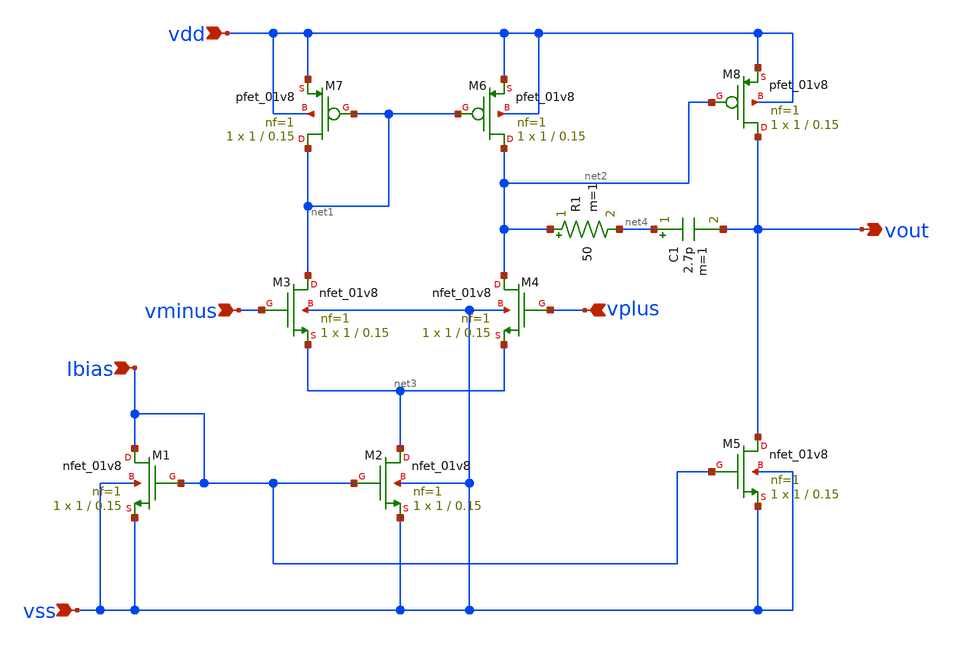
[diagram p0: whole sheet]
** sch_path: Primitives/Operational Amplifier/Xschem Files/sky130_opamp.sch
**.subckt sky130_opamp Ibias vminus vplus vss vdd vout
*.ipin Ibias
*.ipin vminus
*.ipin vplus
*.ipin vss
*.ipin vdd
*.opin vout
XM1 Ibias Ibias vss vss sky130_fd_pr__nfet_01v8 L=0.15 W=1 nf=1 ad='int((1 + 1)/2) * 1 / 1 * 0.29' as='int((1 + 2)/2) * 1 / 1 * 0.29'
+ pd='2*int((1 + 1)/2) * (1 / 1 + 0.29)' ps='2*int((1 + 2)/2) * (1 / 1 + 0.29)' nrd='0.29 / 1 ' nrs='0.29 / 1 '
+ sa=0 sb=0 sd=0 mult=1 m=1
XM2 net3 Ibias vss vss sky130_fd_pr__nfet_01v8 L=0.15 W=1 nf=1 ad='int((1 + 1)/2) * 1 / 1 * 0.29' as='int((1 + 2)/2) * 1 / 1 * 0.29'
+ pd='2*int((1 + 1)/2) * (1 / 1 + 0.29)' ps='2*int((1 + 2)/2) * (1 / 1 + 0.29)' nrd='0.29 / 1 ' nrs='0.29 / 1 '
+ sa=0 sb=0 sd=0 mult=1 m=1
XM3 net1 vminus net3 vss sky130_fd_pr__nfet_01v8 L=0.15 W=1 nf=1 ad='int((1 + 1)/2) * 1 / 1 * 0.29' as='int((1 + 2)/2) * 1 / 1 * 0.29'
+ pd='2*int((1 + 1)/2) * (1 / 1 + 0.29)' ps='2*int((1 + 2)/2) * (1 / 1 + 0.29)' nrd='0.29 / 1 ' nrs='0.29 / 1 '
+ sa=0 sb=0 sd=0 mult=1 m=1
XM4 net2 vplus net3 vss sky130_fd_pr__nfet_01v8 L=0.15 W=1 nf=1 ad='int((1 + 1)/2) * 1 / 1 * 0.29' as='int((1 + 2)/2) * 1 / 1 * 0.29'
+ pd='2*int((1 + 1)/2) * (1 / 1 + 0.29)' ps='2*int((1 + 2)/2) * (1 / 1 + 0.29)' nrd='0.29 / 1 ' nrs='0.29 / 1 '
+ sa=0 sb=0 sd=0 mult=1 m=1
XM5 vout Ibias vss vss sky130_fd_pr__nfet_01v8 L=0.15 W=1 nf=1 ad='int((1 + 1)/2) * 1 / 1 * 0.29' as='int((1 + 2)/2) * 1 / 1 * 0.29'
+ pd='2*int((1 + 1)/2) * (1 / 1 + 0.29)' ps='2*int((1 + 2)/2) * (1 / 1 + 0.29)' nrd='0.29 / 1 ' nrs='0.29 / 1 '
+ sa=0 sb=0 sd=0 mult=1 m=1
XM6 net2 net1 vdd vdd sky130_fd_pr__pfet_01v8 L=0.15 W=1 nf=1 ad='int((1 + 1)/2) * 1 / 1 * 0.29' as='int((1 + 2)/2) * 1 / 1 * 0.29'
+ pd='2*int((1 + 1)/2) * (1 / 1 + 0.29)' ps='2*int((1 + 2)/2) * (1 / 1 + 0.29)' nrd='0.29 / 1 ' nrs='0.29 / 1 '
+ sa=0 sb=0 sd=0 mult=1 m=1
XM7 net1 net1 vdd vdd sky130_fd_pr__pfet_01v8 L=0.15 W=1 nf=1 ad='int((1 + 1)/2) * 1 / 1 * 0.29' as='int((1 + 2)/2) * 1 / 1 * 0.29'
+ pd='2*int((1 + 1)/2) * (1 / 1 + 0.29)' ps='2*int((1 + 2)/2) * (1 / 1 + 0.29)' nrd='0.29 / 1 ' nrs='0.29 / 1 '
+ sa=0 sb=0 sd=0 mult=1 m=1
XM8 vout net2 vdd vdd sky130_fd_pr__pfet_01v8 L=0.15 W=1 nf=1 ad='int((1 + 1)/2) * 1 / 1 * 0.29' as='int((1 + 2)/2) * 1 / 1 * 0.29'
+ pd='2*int((1 + 1)/2) * (1 / 1 + 0.29)' ps='2*int((1 + 2)/2) * (1 / 1 + 0.29)' nrd='0.29 / 1 ' nrs='0.29 / 1 '
+ sa=0 sb=0 sd=0 mult=1 m=1
C1 net4 vout 2.7p m=1
R1 net2 net4 50 m=1
**.ends
.end
